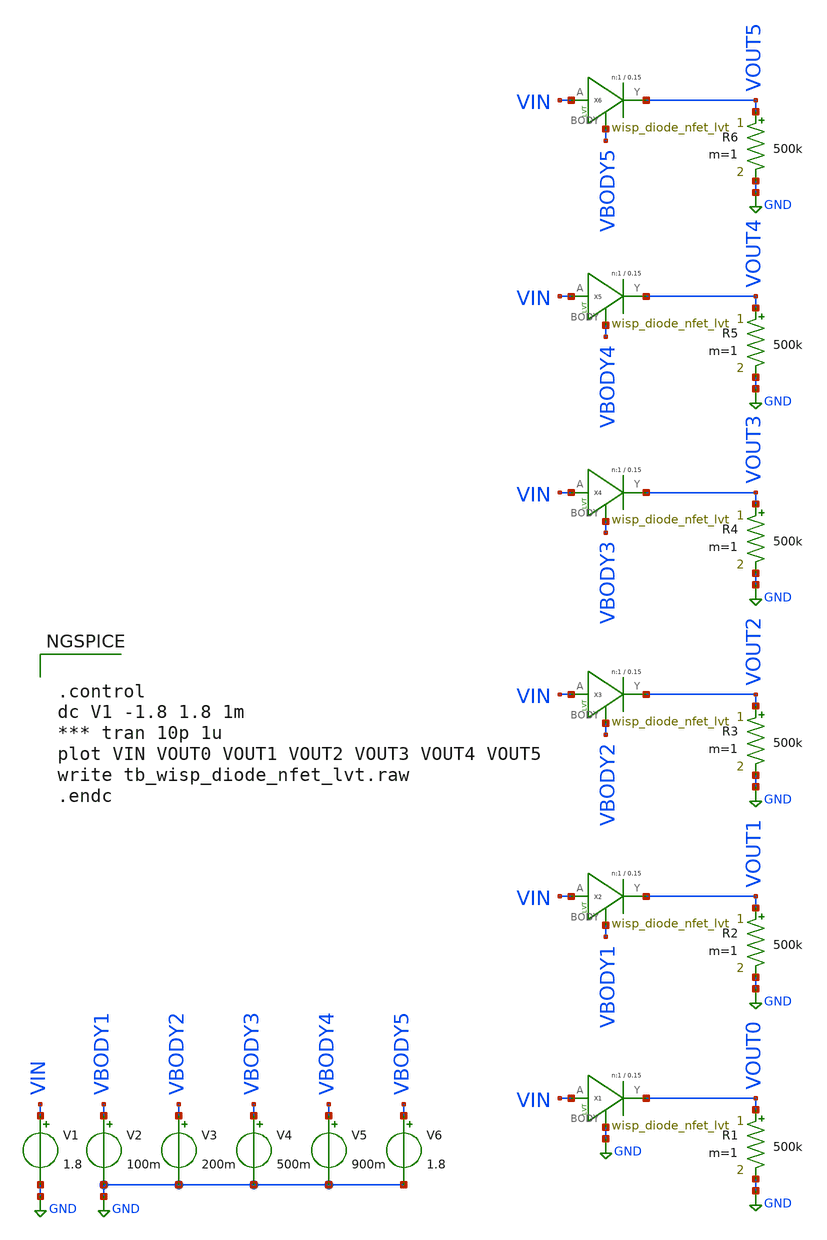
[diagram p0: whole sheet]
** sch_path: tb_wisp_diode_nfet_lvt.sch
**.subckt tb_wisp_diode_nfet_lvt
V1 VIN GND 1.8
X1 VIN VOUT0 GND wisp_diode_nfet_lvt W_N=1 L_N=0.15 m=1
R1 VOUT0 GND 500k m=1
V2 VBODY1 GND 100m
V3 VBODY2 GND 200m
V4 VBODY3 GND 500m
V5 VBODY4 GND 900m
V6 VBODY5 GND 1.8
X2 VIN VOUT1 VBODY1 wisp_diode_nfet_lvt W_N=1 L_N=0.15 m=1
R2 VOUT1 GND 500k m=1
X3 VIN VOUT2 VBODY2 wisp_diode_nfet_lvt W_N=1 L_N=0.15 m=1
R3 VOUT2 GND 500k m=1
X4 VIN VOUT3 VBODY3 wisp_diode_nfet_lvt W_N=1 L_N=0.15 m=1
R4 VOUT3 GND 500k m=1
X5 VIN VOUT4 VBODY4 wisp_diode_nfet_lvt W_N=1 L_N=0.15 m=1
R5 VOUT4 GND 500k m=1
X6 VIN VOUT5 VBODY5 wisp_diode_nfet_lvt W_N=1 L_N=0.15 m=1
R6 VOUT5 GND 500k m=1
**** begin user architecture code


.control
dc V1 -1.8 1.8 1m
*** tran 10p 1u
plot VIN VOUT0 VOUT1 VOUT2 VOUT3 VOUT4 VOUT5
write tb_wisp_diode_nfet_lvt.raw
.endc


 .lib $::SKYWATER_MODELS/sky130.lib.spice tt

.param mc_mm_switch=0
.param mc_pr_switch=1


**** end user architecture code
**.ends

* expanding   symbol:  wisp_diode_nfet_lvt.sym # of pins=3
** sym_path: wisp_diode_nfet_lvt.sym
** sch_path: wisp_diode_nfet_lvt.sch
.subckt wisp_diode_nfet_lvt A Y BODY    W_N=1 L_N=0.15
*.ipin A
*.iopin BODY
*.opin Y
XM1 A A Y BODY sky130_fd_pr__nfet_01v8_lvt L=0.15 W=1 nf=1 ad='int((nf+1)/2) * W/nf * 0.29' as='int((nf+2)/2) * W/nf * 0.29'
+ pd='2*int((nf+1)/2) * (W/nf + 0.29)' ps='2*int((nf+2)/2) * (W/nf + 0.29)' nrd='0.29 / W' nrs='0.29 / W'
+ sa=0 sb=0 sd=0 mult=1 m=1
.ends

.GLOBAL GND
.end
